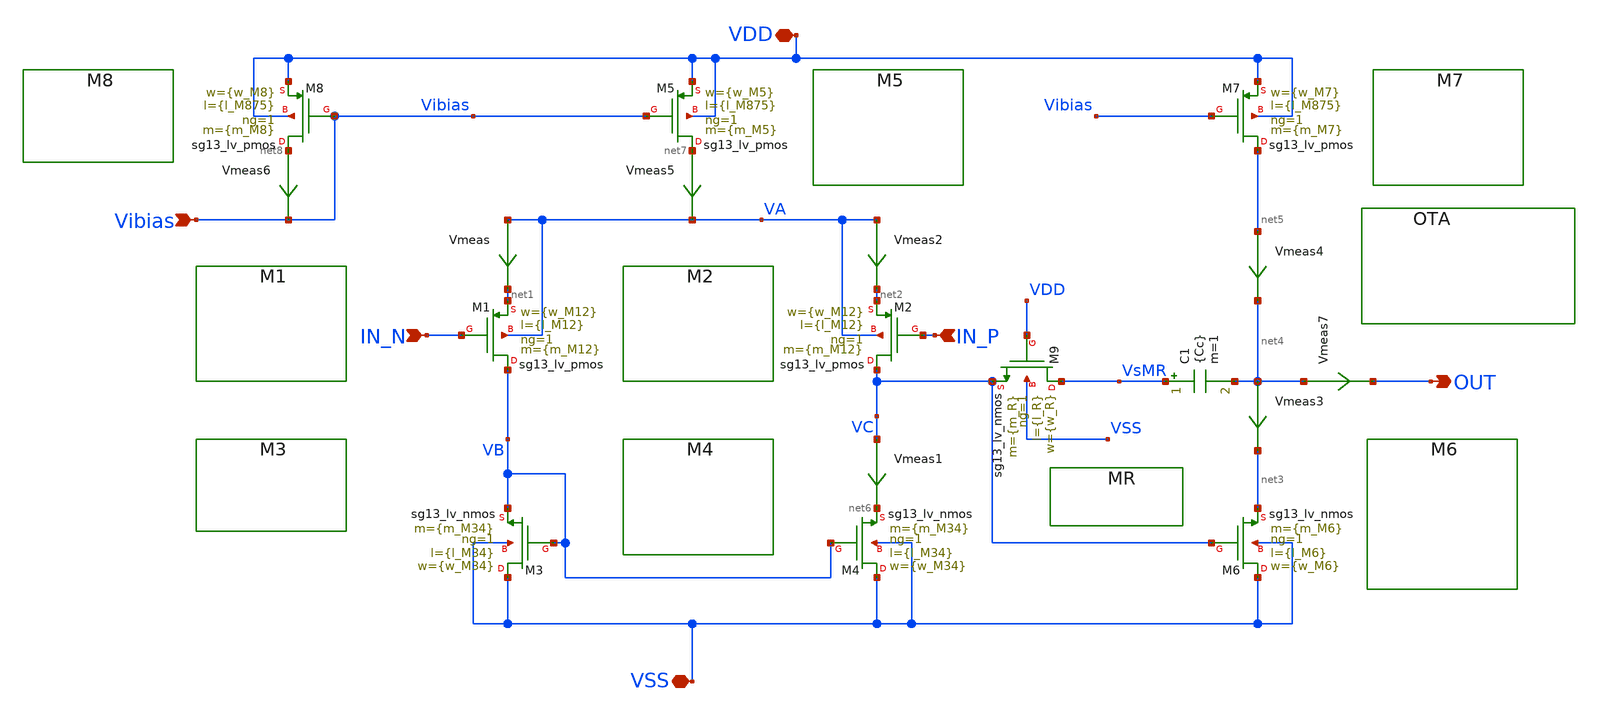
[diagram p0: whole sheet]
** sch_path: xschem/Ayudantias/Ayudantia_2/OTA2_lv_Rc.sch
**.subckt OTA2_lv_Rc IN_N IN_P Vibias OUT VDD VSS
*.ipin IN_N
*.ipin IN_P
*.ipin Vibias
*.opin OUT
*.iopin VDD
*.iopin VSS
XM1 VB IN_N net1 VA sg13_lv_pmos w={w_M12} l={l_M12} ng=1 m={m_M12} mm_ok=1
XM3 VSS VB VB VSS sg13_lv_nmos w={w_M34} l={l_M34} ng=1 m={m_M34} mm_ok=1
XM2 VC IN_P net2 VA sg13_lv_pmos w={w_M12} l={l_M12} ng=1 m={m_M12} mm_ok=1
XM4 VSS VB net6 VSS sg13_lv_nmos w={w_M34} l={l_M34} ng=1 m={m_M34} mm_ok=1
XM5 net7 Vibias VDD VDD sg13_lv_pmos w={w_M5} l={l_M875} ng=1 m={m_M5} mm_ok=1
XM6 VSS VC net3 VSS sg13_lv_nmos w={w_M6} l={l_M6} ng=1 m={m_M6} mm_ok=1
XM7 net5 Vibias VDD VDD sg13_lv_pmos w={w_M7} l={l_M875} ng=1 m={m_M7} mm_ok=1
XM8 net8 Vibias VDD VDD sg13_lv_pmos w={w_M8} l={l_M875} ng=1 m={m_M8} mm_ok=1
XM9 VsMR VDD VC VSS sg13_lv_nmos w={w_R} l={l_R} ng=1 m={m_R} mm_ok=1
C1 VsMR net4 {Cc} m=1
Vmeas VA net1 0
.save i(vmeas)
Vmeas1 VC net6 0
.save i(vmeas1)
Vmeas2 VA net2 0
.save i(vmeas2)
Vmeas3 net4 net3 0
.save i(vmeas3)
Vmeas4 net5 net4 0
.save i(vmeas4)
Vmeas5 net7 VA 0
.save i(vmeas5)
Vmeas6 net8 Vibias 0
.save i(vmeas6)
Vmeas7 net4 OUT 0
.save i(vmeas7)
**.ends
.end
